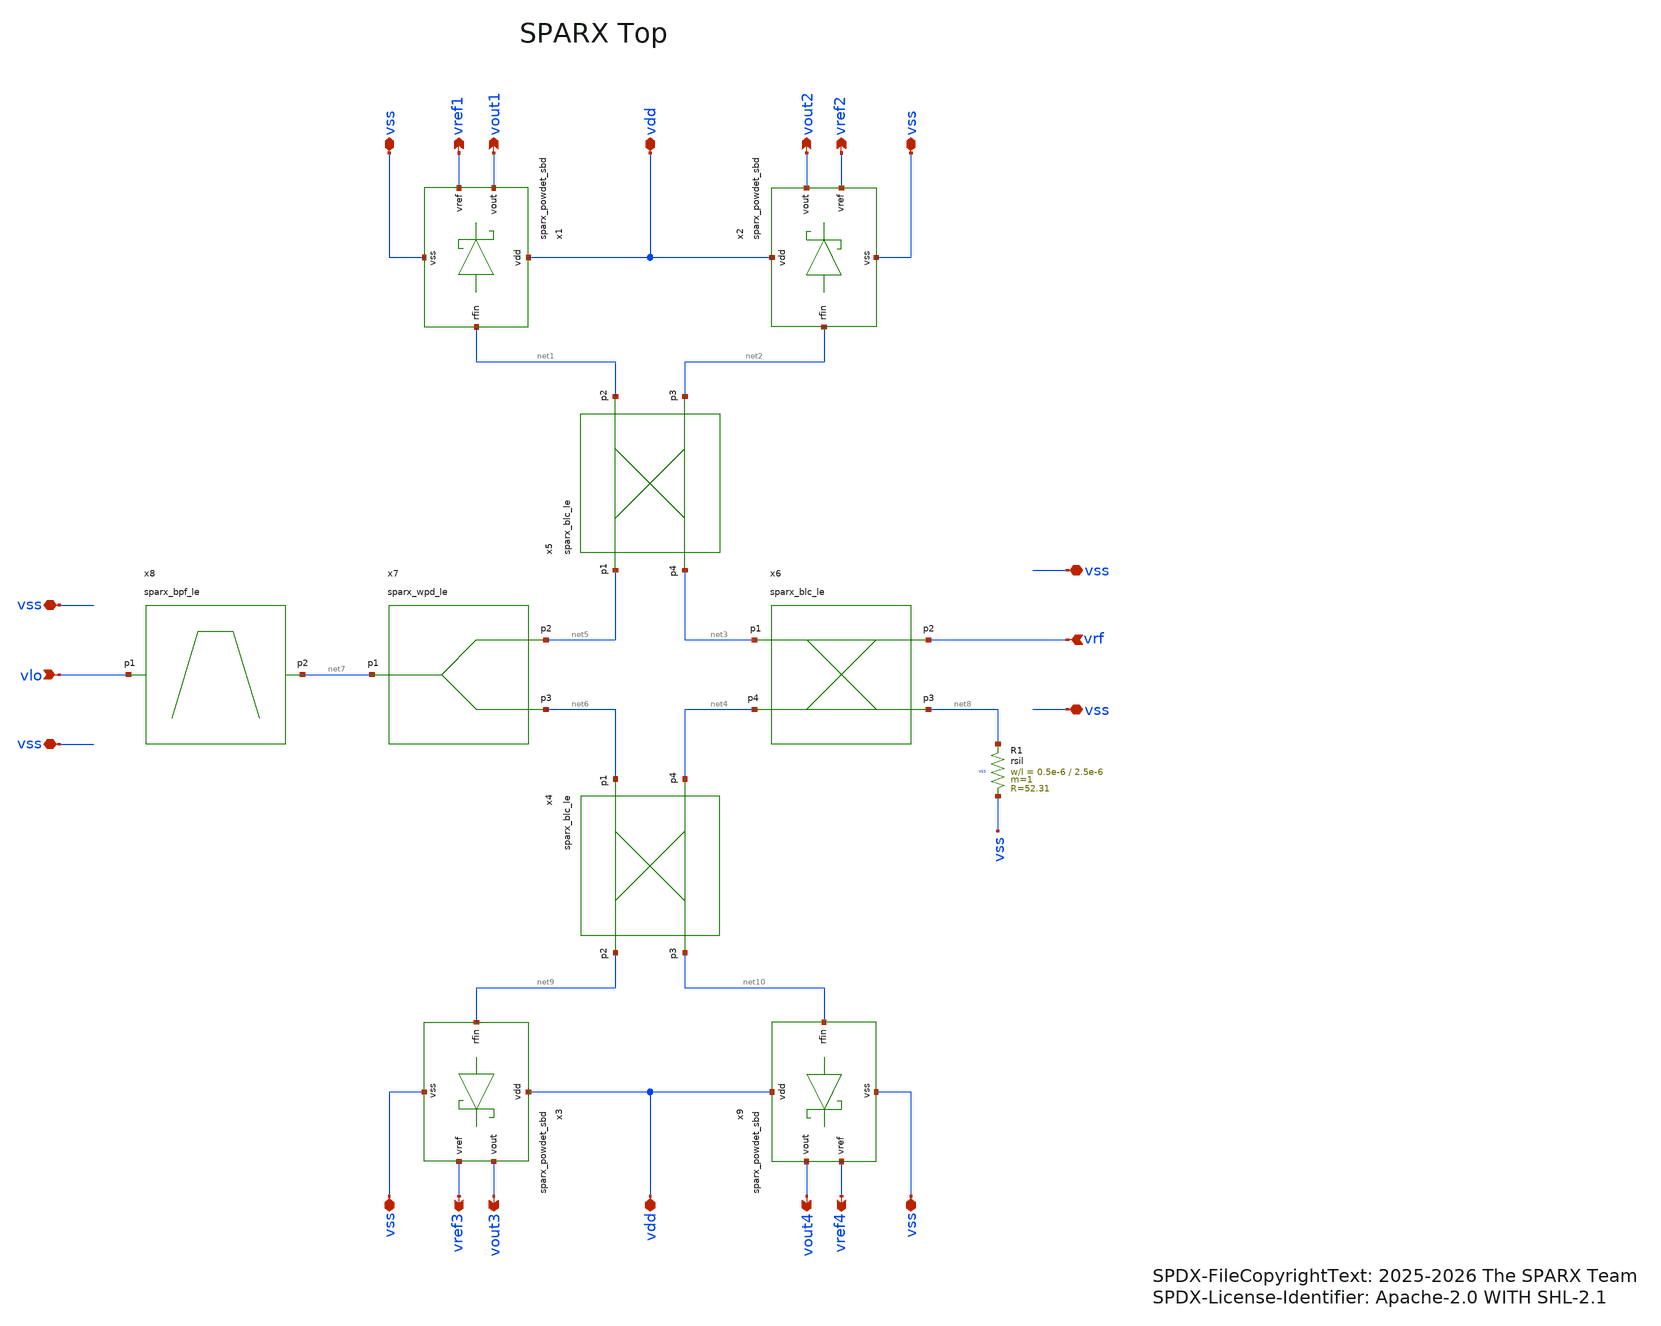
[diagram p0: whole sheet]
** sch_path: schematic/xschem/sparx_top.sch
* SPDX-FileCopyrightText: 2025-2026 The SPARX Team
* SPDX-License-Identifier: Apache-2.0 WITH SHL-2.1
**.subckt sparx_top vrf vout1 vdd vref1 vref2 vout2 vlo vss vss vout3 vdd vref3 vref4 vout4 vss vss
*+ vss vss vss vss
*.ipin vrf
*.opin vout1
*.iopin vdd
*.opin vref1
*.opin vref2
*.opin vout2
*.ipin vlo
*.iopin vss
*.iopin vss
*.opin vout3
*.iopin vdd
*.opin vref3
*.opin vref4
*.opin vout4
*.iopin vss
*.iopin vss
*.iopin vss
*.iopin vss
*.iopin vss
*.iopin vss
x1 vout1 vref1 vdd net1 vss sparx_powdet_sbd
x5 net5 net1 net2 net3 sparx_blc_le
x2 vout2 vref2 vdd net2 vss sparx_powdet_sbd
x6 net3 vrf net8 net4 sparx_blc_le
x7 net7 net5 net6 sparx_wpd_le
x8 vlo net7 sparx_bpf_le
x3 vout3 vref3 vdd net9 vss sparx_powdet_sbd
x4 net6 net9 net10 net4 sparx_blc_le
x9 vout4 vref4 vdd net10 vss sparx_powdet_sbd
XR1 net8 vss vss rsil w=0.5e-6 l=2.5e-6 m=1 mm_ok=1
**.ends
.end
